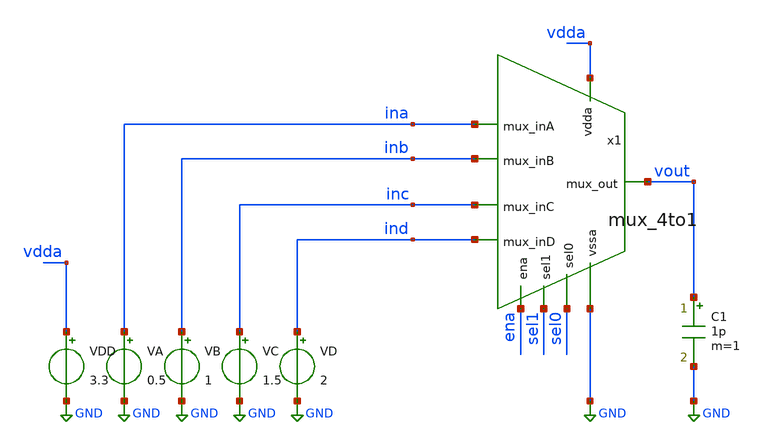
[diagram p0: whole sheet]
** sch_path: xschem/tb_mux_4to1_tran.sch
**.subckt tb_mux_4to1_tran
VB inb GND 1
VA ina GND 0.5
VDD vdda GND 3.3
C1 vout GND 1p m=1
x1 ina sel0 inb sel1 vout inc ind vdda GND ena mux_4to1
VC inc GND 1.5
VD ind GND 2
**** begin user architecture code



.lib /home/ttuser/pdk/sky130A/libs.tech/ngspice/sky130.lib.spice tt

.save all
.option temp=27
vins0 sel0 0 pulse(0 3.3 1us 10NS 10NS 1u 2u 4)
vins1 sel1 0 pulse(0 3.3 2us 10NS 10NS 2u 4u 2)
vinen ena 0 pulse(0 3.3 4.5us 10NS 10NS 4.5u 10u 1)

.control
  tran 1n 10u
  plot v(vout) v(sel0) v(sel1) v(ena)
.endc



**** end user architecture code
**.ends
.GLOBAL GND
.end
